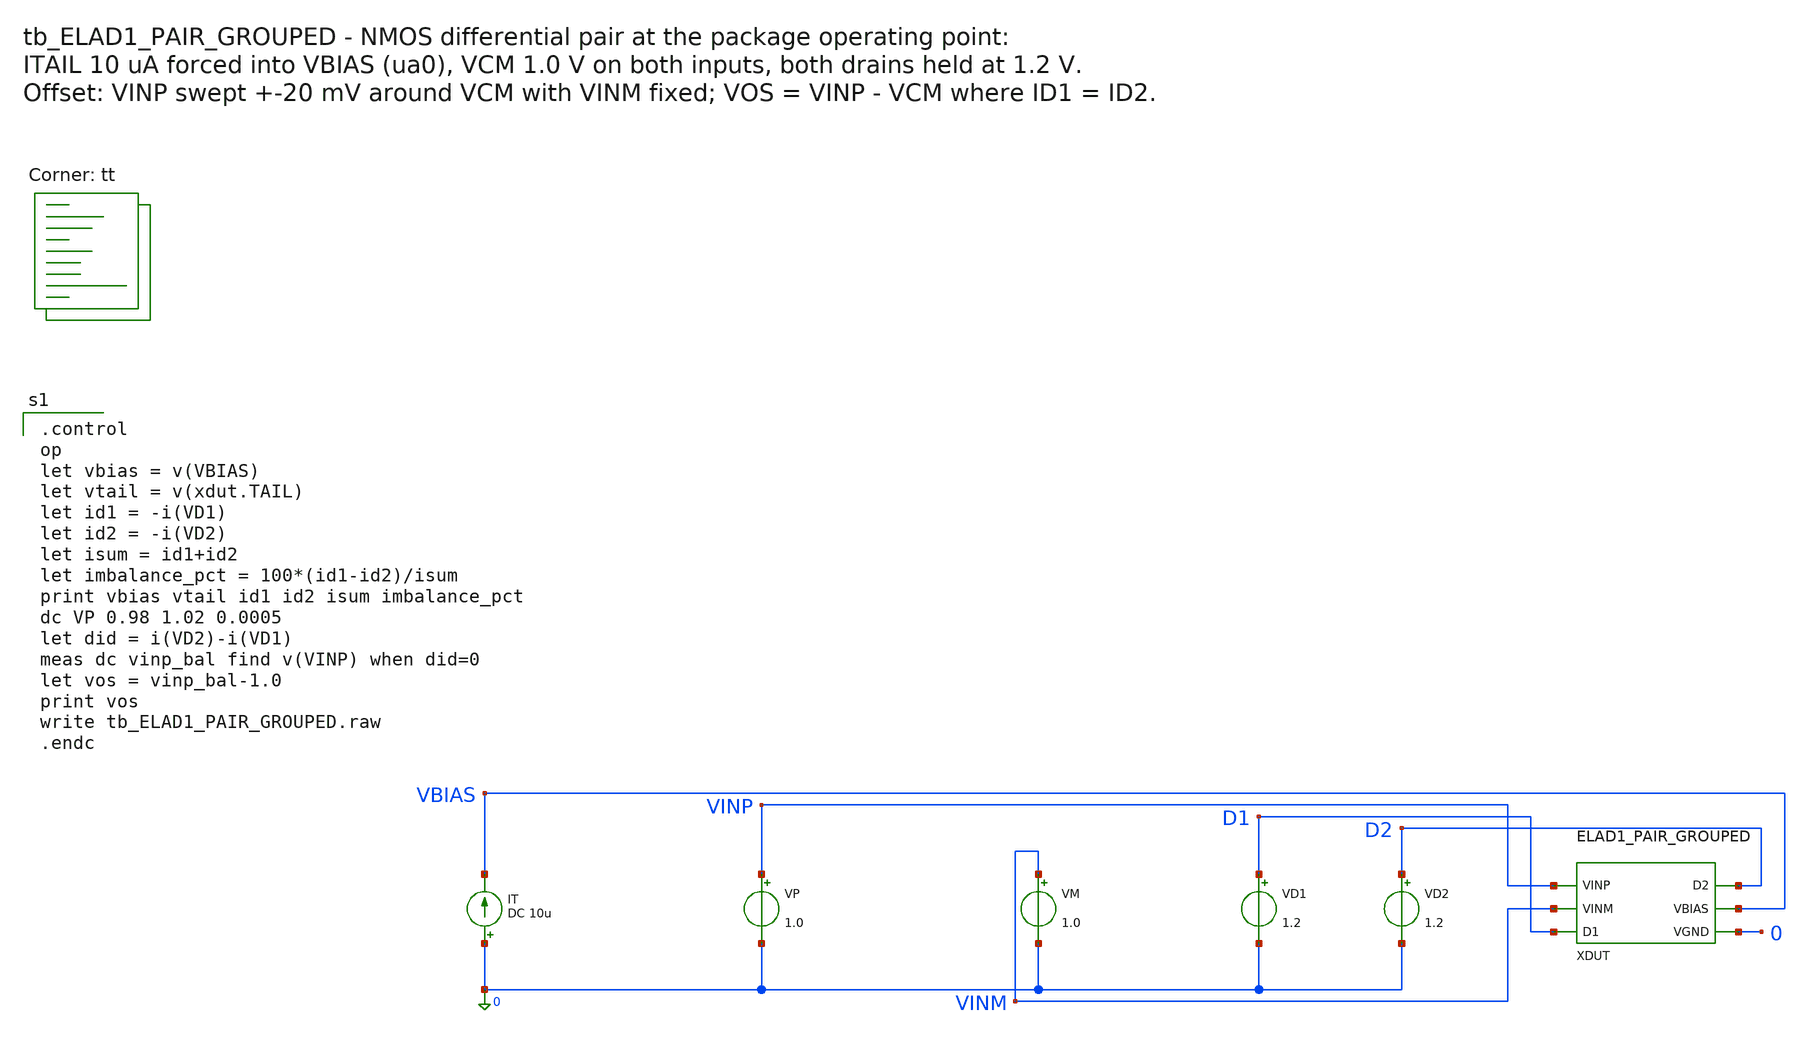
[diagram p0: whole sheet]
** sch_path: cells/ELAD1_PAIR_GROUPED/schematic/tb_ELAD1_PAIR_GROUPED.sch
**.subckt tb_ELAD1_PAIR_GROUPED
IT 0 VBIAS DC 10u
VP VINP 0 1.0
VM VINM 0 1.0
VD1 D1 0 1.2
VD2 D2 0 1.2
XDUT VINP VINM D1 D2 VBIAS 0 ELAD1_PAIR_GROUPED
**** begin user architecture code

.control
op
let vbias = v(VBIAS)
let vtail = v(xdut.TAIL)
let id1 = -i(VD1)
let id2 = -i(VD2)
let isum = id1+id2
let imbalance_pct = 100*(id1-id2)/isum
print vbias vtail id1 id2 isum imbalance_pct
dc VP 0.98 1.02 0.0005
let did = i(VD2)-i(VD1)
meas dc vinp_bal find v(VINP) when did=0
let vos = vinp_bal-1.0
print vos
write tb_ELAD1_PAIR_GROUPED.raw
.endc

.lib $::SKYWATER_MODELS/sky130.lib.spice tt
**** end user architecture code
**.ends

* expanding   symbol:  ELAD1_PAIR_GROUPED.sym # of pins=6
** sym_path: cells/ELAD1_PAIR_GROUPED/schematic/ELAD1_PAIR_GROUPED.sym
** sch_path: cells/ELAD1_PAIR_GROUPED/schematic/ELAD1_PAIR_GROUPED.sch
.subckt ELAD1_PAIR_GROUPED VINP VINM D1 D2 VBIAS VGND
*.iopin VINP
*.iopin VINM
*.iopin D1
*.iopin D2
*.iopin VBIAS
*.iopin VGND
XA0 D1 VINP TAIL VGND sky130_fd_pr__nfet_01v8 L=1 W=2 nf=1 ad='int((1 + 1)/2) * 2 / 1 * 0.29' as='int((1 + 2)/2) * 2 / 1 * 0.29'
+ pd='2*int((1 + 1)/2) * (2 / 1 + 0.29)' ps='2*int((1 + 2)/2) * (2 / 1 + 0.29)' nrd='0.29 / 2 ' nrs='0.29 / 2 '
+ sa=0 sb=0 sd=0 mult=1 m=1
XA1 D1 VINP TAIL VGND sky130_fd_pr__nfet_01v8 L=1 W=2 nf=1 ad='int((1 + 1)/2) * 2 / 1 * 0.29' as='int((1 + 2)/2) * 2 / 1 * 0.29'
+ pd='2*int((1 + 1)/2) * (2 / 1 + 0.29)' ps='2*int((1 + 2)/2) * (2 / 1 + 0.29)' nrd='0.29 / 2 ' nrs='0.29 / 2 '
+ sa=0 sb=0 sd=0 mult=1 m=1
XA2 D1 VINP TAIL VGND sky130_fd_pr__nfet_01v8 L=1 W=2 nf=1 ad='int((1 + 1)/2) * 2 / 1 * 0.29' as='int((1 + 2)/2) * 2 / 1 * 0.29'
+ pd='2*int((1 + 1)/2) * (2 / 1 + 0.29)' ps='2*int((1 + 2)/2) * (2 / 1 + 0.29)' nrd='0.29 / 2 ' nrs='0.29 / 2 '
+ sa=0 sb=0 sd=0 mult=1 m=1
XA3 D1 VINP TAIL VGND sky130_fd_pr__nfet_01v8 L=1 W=2 nf=1 ad='int((1 + 1)/2) * 2 / 1 * 0.29' as='int((1 + 2)/2) * 2 / 1 * 0.29'
+ pd='2*int((1 + 1)/2) * (2 / 1 + 0.29)' ps='2*int((1 + 2)/2) * (2 / 1 + 0.29)' nrd='0.29 / 2 ' nrs='0.29 / 2 '
+ sa=0 sb=0 sd=0 mult=1 m=1
XB0 D2 VINM TAIL VGND sky130_fd_pr__nfet_01v8 L=1 W=2 nf=1 ad='int((1 + 1)/2) * 2 / 1 * 0.29' as='int((1 + 2)/2) * 2 / 1 * 0.29'
+ pd='2*int((1 + 1)/2) * (2 / 1 + 0.29)' ps='2*int((1 + 2)/2) * (2 / 1 + 0.29)' nrd='0.29 / 2 ' nrs='0.29 / 2 '
+ sa=0 sb=0 sd=0 mult=1 m=1
XB1 D2 VINM TAIL VGND sky130_fd_pr__nfet_01v8 L=1 W=2 nf=1 ad='int((1 + 1)/2) * 2 / 1 * 0.29' as='int((1 + 2)/2) * 2 / 1 * 0.29'
+ pd='2*int((1 + 1)/2) * (2 / 1 + 0.29)' ps='2*int((1 + 2)/2) * (2 / 1 + 0.29)' nrd='0.29 / 2 ' nrs='0.29 / 2 '
+ sa=0 sb=0 sd=0 mult=1 m=1
XB2 D2 VINM TAIL VGND sky130_fd_pr__nfet_01v8 L=1 W=2 nf=1 ad='int((1 + 1)/2) * 2 / 1 * 0.29' as='int((1 + 2)/2) * 2 / 1 * 0.29'
+ pd='2*int((1 + 1)/2) * (2 / 1 + 0.29)' ps='2*int((1 + 2)/2) * (2 / 1 + 0.29)' nrd='0.29 / 2 ' nrs='0.29 / 2 '
+ sa=0 sb=0 sd=0 mult=1 m=1
XB3 D2 VINM TAIL VGND sky130_fd_pr__nfet_01v8 L=1 W=2 nf=1 ad='int((1 + 1)/2) * 2 / 1 * 0.29' as='int((1 + 2)/2) * 2 / 1 * 0.29'
+ pd='2*int((1 + 1)/2) * (2 / 1 + 0.29)' ps='2*int((1 + 2)/2) * (2 / 1 + 0.29)' nrd='0.29 / 2 ' nrs='0.29 / 2 '
+ sa=0 sb=0 sd=0 mult=1 m=1
XT0 TAIL VBIAS VGND VGND sky130_fd_pr__nfet_01v8 L=1 W=2 nf=1 ad='int((1 + 1)/2) * 2 / 1 * 0.29' as='int((1 + 2)/2) * 2 / 1 * 0.29'
+ pd='2*int((1 + 1)/2) * (2 / 1 + 0.29)' ps='2*int((1 + 2)/2) * (2 / 1 + 0.29)' nrd='0.29 / 2 ' nrs='0.29 / 2 '
+ sa=0 sb=0 sd=0 mult=1 m=1
XT1 TAIL VBIAS VGND VGND sky130_fd_pr__nfet_01v8 L=1 W=2 nf=1 ad='int((1 + 1)/2) * 2 / 1 * 0.29' as='int((1 + 2)/2) * 2 / 1 * 0.29'
+ pd='2*int((1 + 1)/2) * (2 / 1 + 0.29)' ps='2*int((1 + 2)/2) * (2 / 1 + 0.29)' nrd='0.29 / 2 ' nrs='0.29 / 2 '
+ sa=0 sb=0 sd=0 mult=1 m=1
XT2 TAIL VBIAS VGND VGND sky130_fd_pr__nfet_01v8 L=1 W=2 nf=1 ad='int((1 + 1)/2) * 2 / 1 * 0.29' as='int((1 + 2)/2) * 2 / 1 * 0.29'
+ pd='2*int((1 + 1)/2) * (2 / 1 + 0.29)' ps='2*int((1 + 2)/2) * (2 / 1 + 0.29)' nrd='0.29 / 2 ' nrs='0.29 / 2 '
+ sa=0 sb=0 sd=0 mult=1 m=1
XT3 TAIL VBIAS VGND VGND sky130_fd_pr__nfet_01v8 L=1 W=2 nf=1 ad='int((1 + 1)/2) * 2 / 1 * 0.29' as='int((1 + 2)/2) * 2 / 1 * 0.29'
+ pd='2*int((1 + 1)/2) * (2 / 1 + 0.29)' ps='2*int((1 + 2)/2) * (2 / 1 + 0.29)' nrd='0.29 / 2 ' nrs='0.29 / 2 '
+ sa=0 sb=0 sd=0 mult=1 m=1
XR0 VBIAS VBIAS VGND VGND sky130_fd_pr__nfet_01v8 L=1 W=2 nf=1 ad='int((1 + 1)/2) * 2 / 1 * 0.29' as='int((1 + 2)/2) * 2 / 1 * 0.29'
+ pd='2*int((1 + 1)/2) * (2 / 1 + 0.29)' ps='2*int((1 + 2)/2) * (2 / 1 + 0.29)' nrd='0.29 / 2 ' nrs='0.29 / 2 '
+ sa=0 sb=0 sd=0 mult=1 m=1
XR1 VBIAS VBIAS VGND VGND sky130_fd_pr__nfet_01v8 L=1 W=2 nf=1 ad='int((1 + 1)/2) * 2 / 1 * 0.29' as='int((1 + 2)/2) * 2 / 1 * 0.29'
+ pd='2*int((1 + 1)/2) * (2 / 1 + 0.29)' ps='2*int((1 + 2)/2) * (2 / 1 + 0.29)' nrd='0.29 / 2 ' nrs='0.29 / 2 '
+ sa=0 sb=0 sd=0 mult=1 m=1
XR2 VBIAS VBIAS VGND VGND sky130_fd_pr__nfet_01v8 L=1 W=2 nf=1 ad='int((1 + 1)/2) * 2 / 1 * 0.29' as='int((1 + 2)/2) * 2 / 1 * 0.29'
+ pd='2*int((1 + 1)/2) * (2 / 1 + 0.29)' ps='2*int((1 + 2)/2) * (2 / 1 + 0.29)' nrd='0.29 / 2 ' nrs='0.29 / 2 '
+ sa=0 sb=0 sd=0 mult=1 m=1
XR3 VBIAS VBIAS VGND VGND sky130_fd_pr__nfet_01v8 L=1 W=2 nf=1 ad='int((1 + 1)/2) * 2 / 1 * 0.29' as='int((1 + 2)/2) * 2 / 1 * 0.29'
+ pd='2*int((1 + 1)/2) * (2 / 1 + 0.29)' ps='2*int((1 + 2)/2) * (2 / 1 + 0.29)' nrd='0.29 / 2 ' nrs='0.29 / 2 '
+ sa=0 sb=0 sd=0 mult=1 m=1
XDUM0 VGND VGND VGND VGND sky130_fd_pr__nfet_01v8 L=1 W=2 nf=1 ad='int((1 + 1)/2) * 2 / 1 * 0.29' as='int((1 + 2)/2) * 2 / 1 * 0.29'
+ pd='2*int((1 + 1)/2) * (2 / 1 + 0.29)' ps='2*int((1 + 2)/2) * (2 / 1 + 0.29)' nrd='0.29 / 2 ' nrs='0.29 / 2 '
+ sa=0 sb=0 sd=0 mult=1 m=1
XDUM1 VGND VGND VGND VGND sky130_fd_pr__nfet_01v8 L=1 W=2 nf=1 ad='int((1 + 1)/2) * 2 / 1 * 0.29' as='int((1 + 2)/2) * 2 / 1 * 0.29'
+ pd='2*int((1 + 1)/2) * (2 / 1 + 0.29)' ps='2*int((1 + 2)/2) * (2 / 1 + 0.29)' nrd='0.29 / 2 ' nrs='0.29 / 2 '
+ sa=0 sb=0 sd=0 mult=1 m=1
XDUM2 VGND VGND VGND VGND sky130_fd_pr__nfet_01v8 L=1 W=2 nf=1 ad='int((1 + 1)/2) * 2 / 1 * 0.29' as='int((1 + 2)/2) * 2 / 1 * 0.29'
+ pd='2*int((1 + 1)/2) * (2 / 1 + 0.29)' ps='2*int((1 + 2)/2) * (2 / 1 + 0.29)' nrd='0.29 / 2 ' nrs='0.29 / 2 '
+ sa=0 sb=0 sd=0 mult=1 m=1
XDUM3 VGND VGND VGND VGND sky130_fd_pr__nfet_01v8 L=1 W=2 nf=1 ad='int((1 + 1)/2) * 2 / 1 * 0.29' as='int((1 + 2)/2) * 2 / 1 * 0.29'
+ pd='2*int((1 + 1)/2) * (2 / 1 + 0.29)' ps='2*int((1 + 2)/2) * (2 / 1 + 0.29)' nrd='0.29 / 2 ' nrs='0.29 / 2 '
+ sa=0 sb=0 sd=0 mult=1 m=1
XDUM4 VGND VGND VGND VGND sky130_fd_pr__nfet_01v8 L=1 W=2 nf=1 ad='int((1 + 1)/2) * 2 / 1 * 0.29' as='int((1 + 2)/2) * 2 / 1 * 0.29'
+ pd='2*int((1 + 1)/2) * (2 / 1 + 0.29)' ps='2*int((1 + 2)/2) * (2 / 1 + 0.29)' nrd='0.29 / 2 ' nrs='0.29 / 2 '
+ sa=0 sb=0 sd=0 mult=1 m=1
XDUM5 VGND VGND VGND VGND sky130_fd_pr__nfet_01v8 L=1 W=2 nf=1 ad='int((1 + 1)/2) * 2 / 1 * 0.29' as='int((1 + 2)/2) * 2 / 1 * 0.29'
+ pd='2*int((1 + 1)/2) * (2 / 1 + 0.29)' ps='2*int((1 + 2)/2) * (2 / 1 + 0.29)' nrd='0.29 / 2 ' nrs='0.29 / 2 '
+ sa=0 sb=0 sd=0 mult=1 m=1
XDUM6 VGND VGND VGND VGND sky130_fd_pr__nfet_01v8 L=1 W=2 nf=1 ad='int((1 + 1)/2) * 2 / 1 * 0.29' as='int((1 + 2)/2) * 2 / 1 * 0.29'
+ pd='2*int((1 + 1)/2) * (2 / 1 + 0.29)' ps='2*int((1 + 2)/2) * (2 / 1 + 0.29)' nrd='0.29 / 2 ' nrs='0.29 / 2 '
+ sa=0 sb=0 sd=0 mult=1 m=1
XDUM7 VGND VGND VGND VGND sky130_fd_pr__nfet_01v8 L=1 W=2 nf=1 ad='int((1 + 1)/2) * 2 / 1 * 0.29' as='int((1 + 2)/2) * 2 / 1 * 0.29'
+ pd='2*int((1 + 1)/2) * (2 / 1 + 0.29)' ps='2*int((1 + 2)/2) * (2 / 1 + 0.29)' nrd='0.29 / 2 ' nrs='0.29 / 2 '
+ sa=0 sb=0 sd=0 mult=1 m=1
XDUM8 VGND VGND VGND VGND sky130_fd_pr__nfet_01v8 L=1 W=2 nf=1 ad='int((1 + 1)/2) * 2 / 1 * 0.29' as='int((1 + 2)/2) * 2 / 1 * 0.29'
+ pd='2*int((1 + 1)/2) * (2 / 1 + 0.29)' ps='2*int((1 + 2)/2) * (2 / 1 + 0.29)' nrd='0.29 / 2 ' nrs='0.29 / 2 '
+ sa=0 sb=0 sd=0 mult=1 m=1
XDUM9 VGND VGND VGND VGND sky130_fd_pr__nfet_01v8 L=1 W=2 nf=1 ad='int((1 + 1)/2) * 2 / 1 * 0.29' as='int((1 + 2)/2) * 2 / 1 * 0.29'
+ pd='2*int((1 + 1)/2) * (2 / 1 + 0.29)' ps='2*int((1 + 2)/2) * (2 / 1 + 0.29)' nrd='0.29 / 2 ' nrs='0.29 / 2 '
+ sa=0 sb=0 sd=0 mult=1 m=1
XDUM10 VGND VGND VGND VGND sky130_fd_pr__nfet_01v8 L=1 W=2 nf=1 ad='int((1 + 1)/2) * 2 / 1 * 0.29' as='int((1 + 2)/2) * 2 / 1 * 0.29'
+ pd='2*int((1 + 1)/2) * (2 / 1 + 0.29)' ps='2*int((1 + 2)/2) * (2 / 1 + 0.29)' nrd='0.29 / 2 ' nrs='0.29 / 2 '
+ sa=0 sb=0 sd=0 mult=1 m=1
XDUM11 VGND VGND VGND VGND sky130_fd_pr__nfet_01v8 L=1 W=2 nf=1 ad='int((1 + 1)/2) * 2 / 1 * 0.29' as='int((1 + 2)/2) * 2 / 1 * 0.29'
+ pd='2*int((1 + 1)/2) * (2 / 1 + 0.29)' ps='2*int((1 + 2)/2) * (2 / 1 + 0.29)' nrd='0.29 / 2 ' nrs='0.29 / 2 '
+ sa=0 sb=0 sd=0 mult=1 m=1
XDUM12 VGND VGND VGND VGND sky130_fd_pr__nfet_01v8 L=1 W=2 nf=1 ad='int((1 + 1)/2) * 2 / 1 * 0.29' as='int((1 + 2)/2) * 2 / 1 * 0.29'
+ pd='2*int((1 + 1)/2) * (2 / 1 + 0.29)' ps='2*int((1 + 2)/2) * (2 / 1 + 0.29)' nrd='0.29 / 2 ' nrs='0.29 / 2 '
+ sa=0 sb=0 sd=0 mult=1 m=1
XDUM13 VGND VGND VGND VGND sky130_fd_pr__nfet_01v8 L=1 W=2 nf=1 ad='int((1 + 1)/2) * 2 / 1 * 0.29' as='int((1 + 2)/2) * 2 / 1 * 0.29'
+ pd='2*int((1 + 1)/2) * (2 / 1 + 0.29)' ps='2*int((1 + 2)/2) * (2 / 1 + 0.29)' nrd='0.29 / 2 ' nrs='0.29 / 2 '
+ sa=0 sb=0 sd=0 mult=1 m=1
XDUM14 VGND VGND VGND VGND sky130_fd_pr__nfet_01v8 L=1 W=2 nf=1 ad='int((1 + 1)/2) * 2 / 1 * 0.29' as='int((1 + 2)/2) * 2 / 1 * 0.29'
+ pd='2*int((1 + 1)/2) * (2 / 1 + 0.29)' ps='2*int((1 + 2)/2) * (2 / 1 + 0.29)' nrd='0.29 / 2 ' nrs='0.29 / 2 '
+ sa=0 sb=0 sd=0 mult=1 m=1
XDUM15 VGND VGND VGND VGND sky130_fd_pr__nfet_01v8 L=1 W=2 nf=1 ad='int((1 + 1)/2) * 2 / 1 * 0.29' as='int((1 + 2)/2) * 2 / 1 * 0.29'
+ pd='2*int((1 + 1)/2) * (2 / 1 + 0.29)' ps='2*int((1 + 2)/2) * (2 / 1 + 0.29)' nrd='0.29 / 2 ' nrs='0.29 / 2 '
+ sa=0 sb=0 sd=0 mult=1 m=1
XDUM16 VGND VGND VGND VGND sky130_fd_pr__nfet_01v8 L=1 W=2 nf=1 ad='int((1 + 1)/2) * 2 / 1 * 0.29' as='int((1 + 2)/2) * 2 / 1 * 0.29'
+ pd='2*int((1 + 1)/2) * (2 / 1 + 0.29)' ps='2*int((1 + 2)/2) * (2 / 1 + 0.29)' nrd='0.29 / 2 ' nrs='0.29 / 2 '
+ sa=0 sb=0 sd=0 mult=1 m=1
XDUM17 VGND VGND VGND VGND sky130_fd_pr__nfet_01v8 L=1 W=2 nf=1 ad='int((1 + 1)/2) * 2 / 1 * 0.29' as='int((1 + 2)/2) * 2 / 1 * 0.29'
+ pd='2*int((1 + 1)/2) * (2 / 1 + 0.29)' ps='2*int((1 + 2)/2) * (2 / 1 + 0.29)' nrd='0.29 / 2 ' nrs='0.29 / 2 '
+ sa=0 sb=0 sd=0 mult=1 m=1
XDUM18 VGND VGND VGND VGND sky130_fd_pr__nfet_01v8 L=1 W=2 nf=1 ad='int((1 + 1)/2) * 2 / 1 * 0.29' as='int((1 + 2)/2) * 2 / 1 * 0.29'
+ pd='2*int((1 + 1)/2) * (2 / 1 + 0.29)' ps='2*int((1 + 2)/2) * (2 / 1 + 0.29)' nrd='0.29 / 2 ' nrs='0.29 / 2 '
+ sa=0 sb=0 sd=0 mult=1 m=1
XDUM19 VGND VGND VGND VGND sky130_fd_pr__nfet_01v8 L=1 W=2 nf=1 ad='int((1 + 1)/2) * 2 / 1 * 0.29' as='int((1 + 2)/2) * 2 / 1 * 0.29'
+ pd='2*int((1 + 1)/2) * (2 / 1 + 0.29)' ps='2*int((1 + 2)/2) * (2 / 1 + 0.29)' nrd='0.29 / 2 ' nrs='0.29 / 2 '
+ sa=0 sb=0 sd=0 mult=1 m=1
XDUM20 VGND VGND VGND VGND sky130_fd_pr__nfet_01v8 L=1 W=2 nf=1 ad='int((1 + 1)/2) * 2 / 1 * 0.29' as='int((1 + 2)/2) * 2 / 1 * 0.29'
+ pd='2*int((1 + 1)/2) * (2 / 1 + 0.29)' ps='2*int((1 + 2)/2) * (2 / 1 + 0.29)' nrd='0.29 / 2 ' nrs='0.29 / 2 '
+ sa=0 sb=0 sd=0 mult=1 m=1
XDUM21 VGND VGND VGND VGND sky130_fd_pr__nfet_01v8 L=1 W=2 nf=1 ad='int((1 + 1)/2) * 2 / 1 * 0.29' as='int((1 + 2)/2) * 2 / 1 * 0.29'
+ pd='2*int((1 + 1)/2) * (2 / 1 + 0.29)' ps='2*int((1 + 2)/2) * (2 / 1 + 0.29)' nrd='0.29 / 2 ' nrs='0.29 / 2 '
+ sa=0 sb=0 sd=0 mult=1 m=1
XDUM22 VGND VGND VGND VGND sky130_fd_pr__nfet_01v8 L=1 W=2 nf=1 ad='int((1 + 1)/2) * 2 / 1 * 0.29' as='int((1 + 2)/2) * 2 / 1 * 0.29'
+ pd='2*int((1 + 1)/2) * (2 / 1 + 0.29)' ps='2*int((1 + 2)/2) * (2 / 1 + 0.29)' nrd='0.29 / 2 ' nrs='0.29 / 2 '
+ sa=0 sb=0 sd=0 mult=1 m=1
XDUM23 VGND VGND VGND VGND sky130_fd_pr__nfet_01v8 L=1 W=2 nf=1 ad='int((1 + 1)/2) * 2 / 1 * 0.29' as='int((1 + 2)/2) * 2 / 1 * 0.29'
+ pd='2*int((1 + 1)/2) * (2 / 1 + 0.29)' ps='2*int((1 + 2)/2) * (2 / 1 + 0.29)' nrd='0.29 / 2 ' nrs='0.29 / 2 '
+ sa=0 sb=0 sd=0 mult=1 m=1
XDUM24 VGND VGND VGND VGND sky130_fd_pr__nfet_01v8 L=1 W=2 nf=1 ad='int((1 + 1)/2) * 2 / 1 * 0.29' as='int((1 + 2)/2) * 2 / 1 * 0.29'
+ pd='2*int((1 + 1)/2) * (2 / 1 + 0.29)' ps='2*int((1 + 2)/2) * (2 / 1 + 0.29)' nrd='0.29 / 2 ' nrs='0.29 / 2 '
+ sa=0 sb=0 sd=0 mult=1 m=1
XDUM25 VGND VGND VGND VGND sky130_fd_pr__nfet_01v8 L=1 W=2 nf=1 ad='int((1 + 1)/2) * 2 / 1 * 0.29' as='int((1 + 2)/2) * 2 / 1 * 0.29'
+ pd='2*int((1 + 1)/2) * (2 / 1 + 0.29)' ps='2*int((1 + 2)/2) * (2 / 1 + 0.29)' nrd='0.29 / 2 ' nrs='0.29 / 2 '
+ sa=0 sb=0 sd=0 mult=1 m=1
XDUM26 VGND VGND VGND VGND sky130_fd_pr__nfet_01v8 L=1 W=2 nf=1 ad='int((1 + 1)/2) * 2 / 1 * 0.29' as='int((1 + 2)/2) * 2 / 1 * 0.29'
+ pd='2*int((1 + 1)/2) * (2 / 1 + 0.29)' ps='2*int((1 + 2)/2) * (2 / 1 + 0.29)' nrd='0.29 / 2 ' nrs='0.29 / 2 '
+ sa=0 sb=0 sd=0 mult=1 m=1
XDUM27 VGND VGND VGND VGND sky130_fd_pr__nfet_01v8 L=1 W=2 nf=1 ad='int((1 + 1)/2) * 2 / 1 * 0.29' as='int((1 + 2)/2) * 2 / 1 * 0.29'
+ pd='2*int((1 + 1)/2) * (2 / 1 + 0.29)' ps='2*int((1 + 2)/2) * (2 / 1 + 0.29)' nrd='0.29 / 2 ' nrs='0.29 / 2 '
+ sa=0 sb=0 sd=0 mult=1 m=1
XDUM28 VGND VGND VGND VGND sky130_fd_pr__nfet_01v8 L=1 W=2 nf=1 ad='int((1 + 1)/2) * 2 / 1 * 0.29' as='int((1 + 2)/2) * 2 / 1 * 0.29'
+ pd='2*int((1 + 1)/2) * (2 / 1 + 0.29)' ps='2*int((1 + 2)/2) * (2 / 1 + 0.29)' nrd='0.29 / 2 ' nrs='0.29 / 2 '
+ sa=0 sb=0 sd=0 mult=1 m=1
XDUM29 VGND VGND VGND VGND sky130_fd_pr__nfet_01v8 L=1 W=2 nf=1 ad='int((1 + 1)/2) * 2 / 1 * 0.29' as='int((1 + 2)/2) * 2 / 1 * 0.29'
+ pd='2*int((1 + 1)/2) * (2 / 1 + 0.29)' ps='2*int((1 + 2)/2) * (2 / 1 + 0.29)' nrd='0.29 / 2 ' nrs='0.29 / 2 '
+ sa=0 sb=0 sd=0 mult=1 m=1
XDUM30 VGND VGND VGND VGND sky130_fd_pr__nfet_01v8 L=1 W=2 nf=1 ad='int((1 + 1)/2) * 2 / 1 * 0.29' as='int((1 + 2)/2) * 2 / 1 * 0.29'
+ pd='2*int((1 + 1)/2) * (2 / 1 + 0.29)' ps='2*int((1 + 2)/2) * (2 / 1 + 0.29)' nrd='0.29 / 2 ' nrs='0.29 / 2 '
+ sa=0 sb=0 sd=0 mult=1 m=1
XDUM31 VGND VGND VGND VGND sky130_fd_pr__nfet_01v8 L=1 W=2 nf=1 ad='int((1 + 1)/2) * 2 / 1 * 0.29' as='int((1 + 2)/2) * 2 / 1 * 0.29'
+ pd='2*int((1 + 1)/2) * (2 / 1 + 0.29)' ps='2*int((1 + 2)/2) * (2 / 1 + 0.29)' nrd='0.29 / 2 ' nrs='0.29 / 2 '
+ sa=0 sb=0 sd=0 mult=1 m=1
.ends

.GLOBAL VGND
.end
